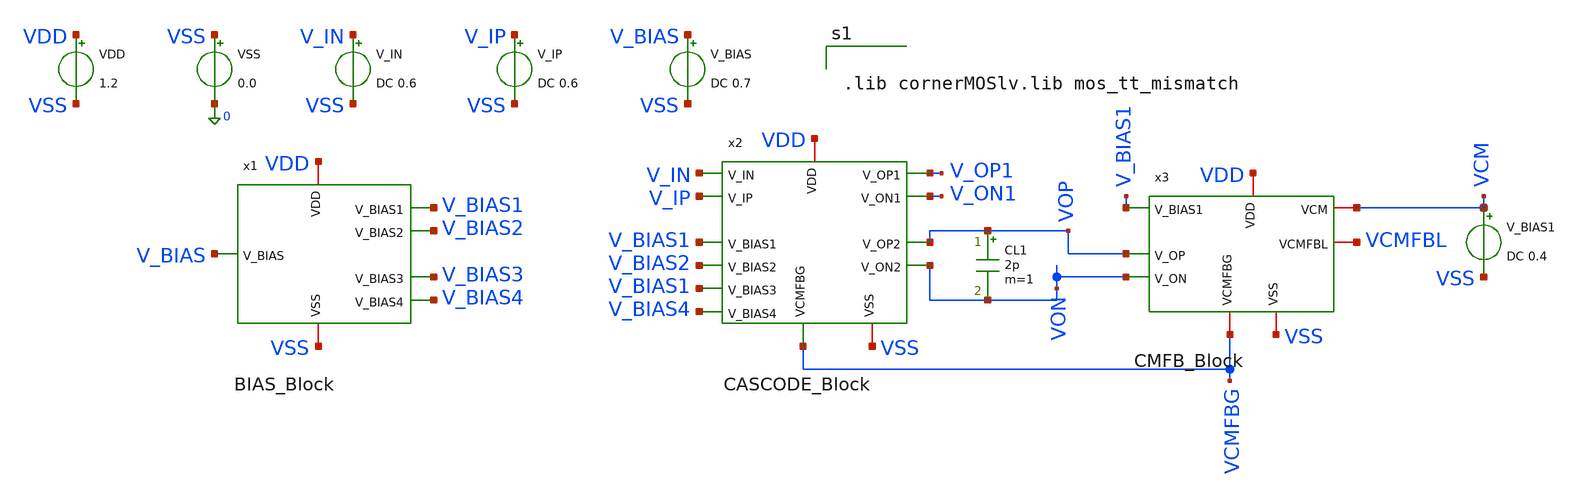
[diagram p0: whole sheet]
** sch_path: two-stage-ota-with-cmfb/Simulation/TEST_MONTE_CARLO.sch
**.subckt TEST_MONTE_CARLO
VDD VDD VSS 1.2
VSS VSS 0 0.0
V_IN V_IN VSS DC 0.6
V_IP V_IP VSS DC 0.6
V_BIAS V_BIAS VSS DC 0.7
V_BIAS1 VCM VSS DC 0.4
CL1 VOP VON 2p m=1
x1 VSS V_BIAS4 V_BIAS2 V_BIAS3 VDD V_BIAS1 V_BIAS BIAS_Block
x2 VDD V_BIAS1 V_IN V_IP V_BIAS2 V_ON1 V_OP1 V_BIAS1 VON VOP VCMFBG V_BIAS4 VSS CASCODE_Block
x3 VDD V_BIAS1 VCM VOP VON VCMFBL VCMFBG VSS CMFB_Block
**** begin user architecture code


.lib cornerMOSlv.lib mos_tt_mismatch




* ==============================================================================
* MUC F.2: 200-POINT MONTE CARLO - TAP TRUNG VOS, DC GAIN VA VOCM
* ==============================================================================

.control
set color0=white
set color1=black

let run = 1
let mc_runs = 200

* Tao plot scratch rieng de chua du lieu thong ke
set curplot = new
set scratch = $curplot

* Khoi tao dung 3 vector muc tieu va 1 vector truc hoanh
let vos_vec  = vector(mc_runs)
let gain_vec = vector(mc_runs)
let vocm_vec = vector(mc_runs)
let run_vec  = vector(mc_runs)

echo '=========================================================================='
echo '  BAT DAU CHAY 200 DIEM MONTE CARLO (VOS, DC GAIN, VOCM)                 '
echo '=========================================================================='

dowhile run <= mc_runs
  echo '--> Monte Carlo run:' $&run '/' $&mc_runs
  reset

  * 1. DC Operating Point: Lay Vocm va do lech dien ap DC ngo ra
  op
  set opplot = $curplot

  * 2. AC Sweep tan so thap de do chinh xac DC Gain theo tung mismatch
  ac dec 2 1 10
  set acplot = $curplot

  * Tinh toan tai plot DC OP
  setplot $opplot
  let v_out_diff_dc = v(vop) - v(von)
  let v_ocm_val     = (v(vop) + v(von)) / 2

  * Tinh toan do loi vi sai tai plot AC
  setplot $acplot
  let diff_out_ac = mag(v(vop) - v(von))
  let diff_in_ac  = mag(v(v_ip) - v(v_in))

  * Tinh he so khuech dai tuyen tinh va dB
  if (diff_in_ac[0] > 1e-6)
    let a_diff_lin = diff_out_ac[0] / diff_in_ac[0]
  else
    let a_diff_lin = 5800.0
  end
  let gain_val_db = db(a_diff_lin)

  * Ghi du lieu sang plot scratch
  setplot $scratch
  let run_vec[run-1]  = run
  let vocm_vec[run-1] = {$opplot}.v_ocm_val
  let gain_vec[run-1] = {$acplot}.gain_val_db
  * Vos quy doi ve ngo vao: Vos = Vout_diff_dc / A_diff_lin (mV)
  let vos_vec[run-1]  = ({$opplot}.v_out_diff_dc / {$acplot}.a_diff_lin) * 1e3

  let run = run + 1
end

* Tinh toan gia tri trung binh (Mean) va do lech chuan (Std Dev)
setplot $scratch

let mean_vos  = mean(vos_vec)
let std_vos   = sqrt(mean((vos_vec - mean_vos) * (vos_vec - mean_vos)))

let mean_gain = mean(gain_vec)
let std_gain  = sqrt(mean((gain_vec - mean_gain) * (gain_vec - mean_gain)))

let mean_vocm = mean(vocm_vec)
let std_vocm  = sqrt(mean((vocm_vec - mean_vocm) * (vocm_vec - mean_vocm)))

echo '=========================================================================='
echo '               KET QUA THONG KE 200 DIEM MONTE CARLO                      '
echo '=========================================================================='
echo '1. INPUT OFFSET VOLTAGE Vos (mV):'
print mean_vos std_vos
echo '--------------------------------------------------------------------------'
echo '2. DC GAIN (dB):'
print mean_gain std_gain
echo '--------------------------------------------------------------------------'
echo '3. OUTPUT COMMON-MODE VOLTAGE Vocm (V):'
print mean_vocm std_vocm
echo '=========================================================================='

* Luu du lieu tho ra file
write mc_results_final.raw vos_vec gain_vec vocm_vec run_vec

* Ve 3 do thi phan bo theo thu tu run
plot vos_vec vs run_vec ylabel 'Vos (mV)' xlabel 'Run Number' title 'Input Offset Voltage Vos across 200 Runs'
plot gain_vec vs run_vec ylabel 'Gain (dB)' xlabel 'Run Number' title 'DC Gain across 200 Runs'
plot vocm_vec vs run_vec ylabel 'Vocm (V)' xlabel 'Run Number' title 'Output CM Voltage Vocm across 200 Runs'

.endc


**** end user architecture code
**.ends
.end
